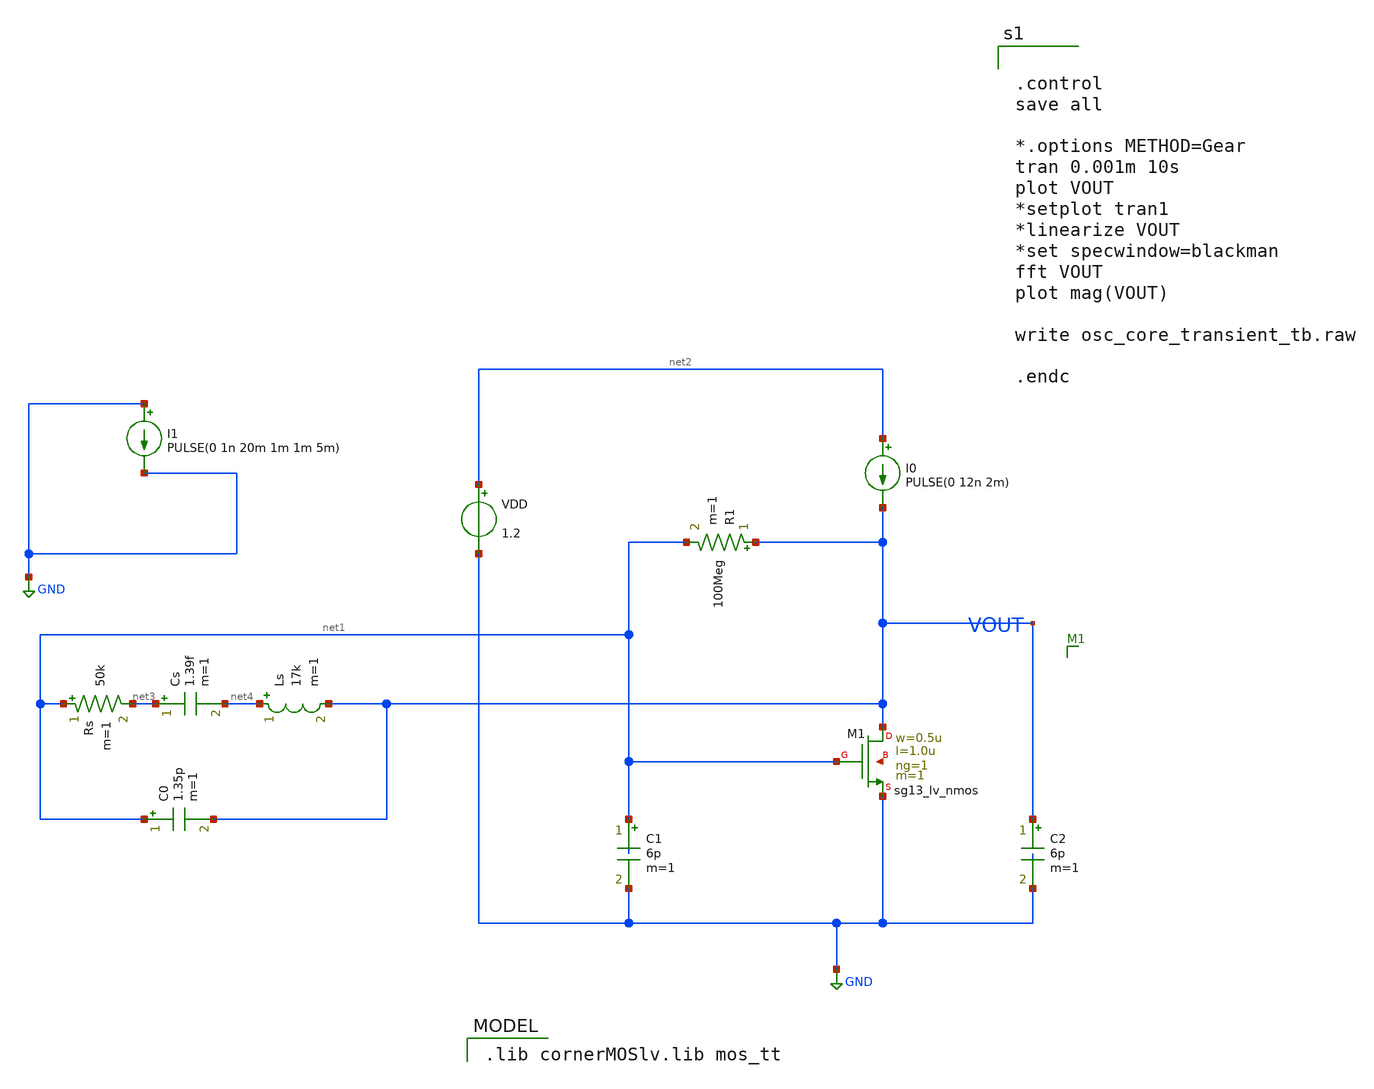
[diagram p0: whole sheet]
** sch_path: osc_core_transient_tb.sch
**.subckt osc_core_transient_tb
XM1 VOUT net1 GND net5 sg13_lv_nmos w=0.5u l=1.0u ng=1 m=1 mm_ok=1
C1 net1 GND 6p m=1
C2 VOUT GND 6p m=1
R1 VOUT net1 100Meg m=1
I0 net2 VOUT PULSE(0 12n 2m)
I1 GND GND PULSE(0 1n 20m 1m 1m 5m)
Rs net1 net3 50k m=1
Cs net3 net4 1.39f m=1
C0 net1 VOUT 1.35p m=1
Ls net4 VOUT 17k m=1
VDD net2 GND 1.2
**** begin user architecture code


.control
save all

*.options METHOD=Gear
tran 0.001m 10s
plot VOUT
*setplot tran1
*linearize VOUT
*set specwindow=blackman
fft VOUT
plot mag(VOUT)

write osc_core_transient_tb.raw

.endc


 .lib cornerMOSlv.lib mos_tt

**** end user architecture code
**.ends
.GLOBAL GND
.end
